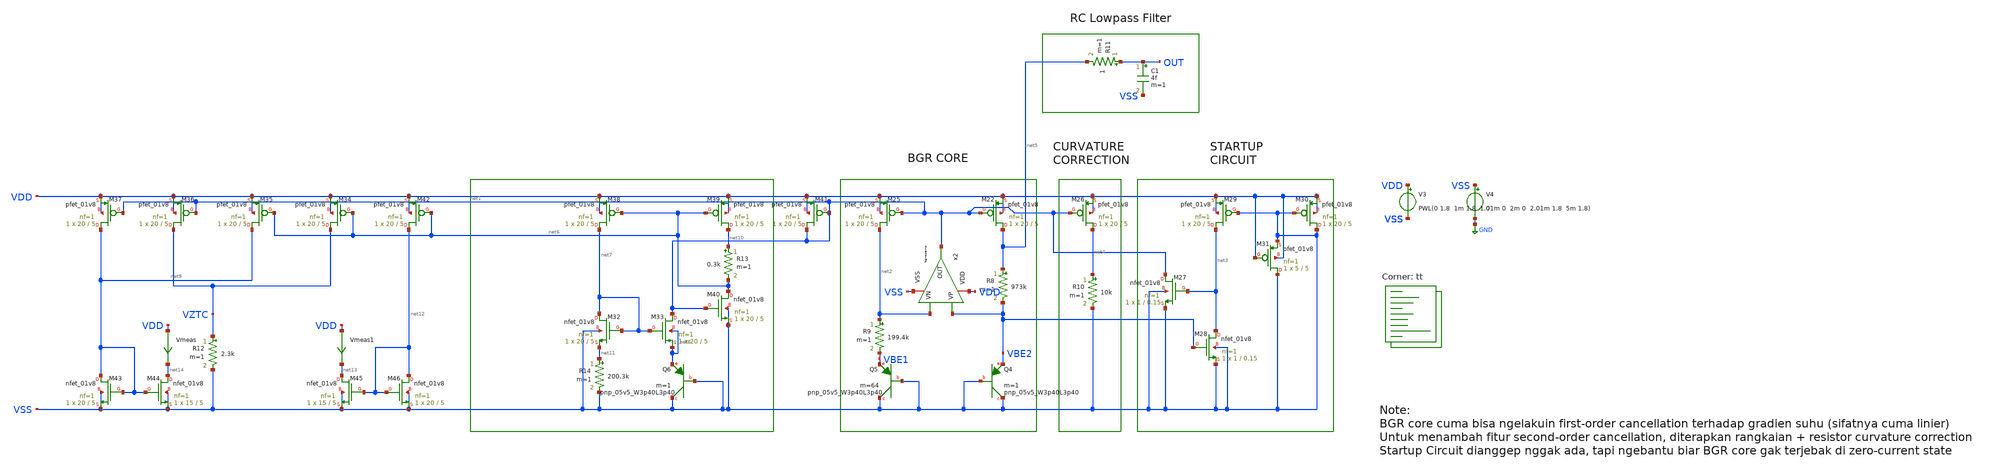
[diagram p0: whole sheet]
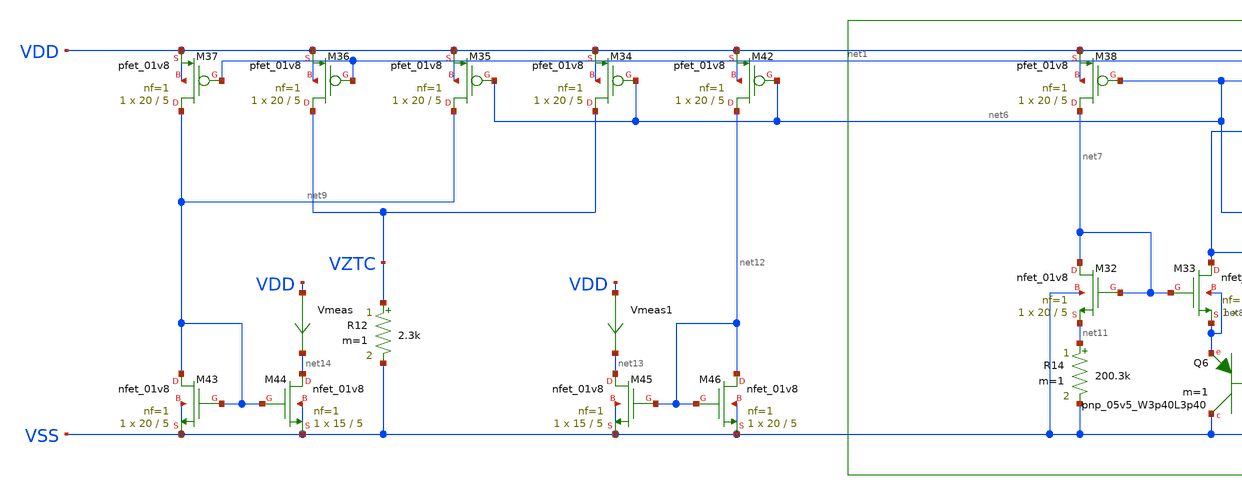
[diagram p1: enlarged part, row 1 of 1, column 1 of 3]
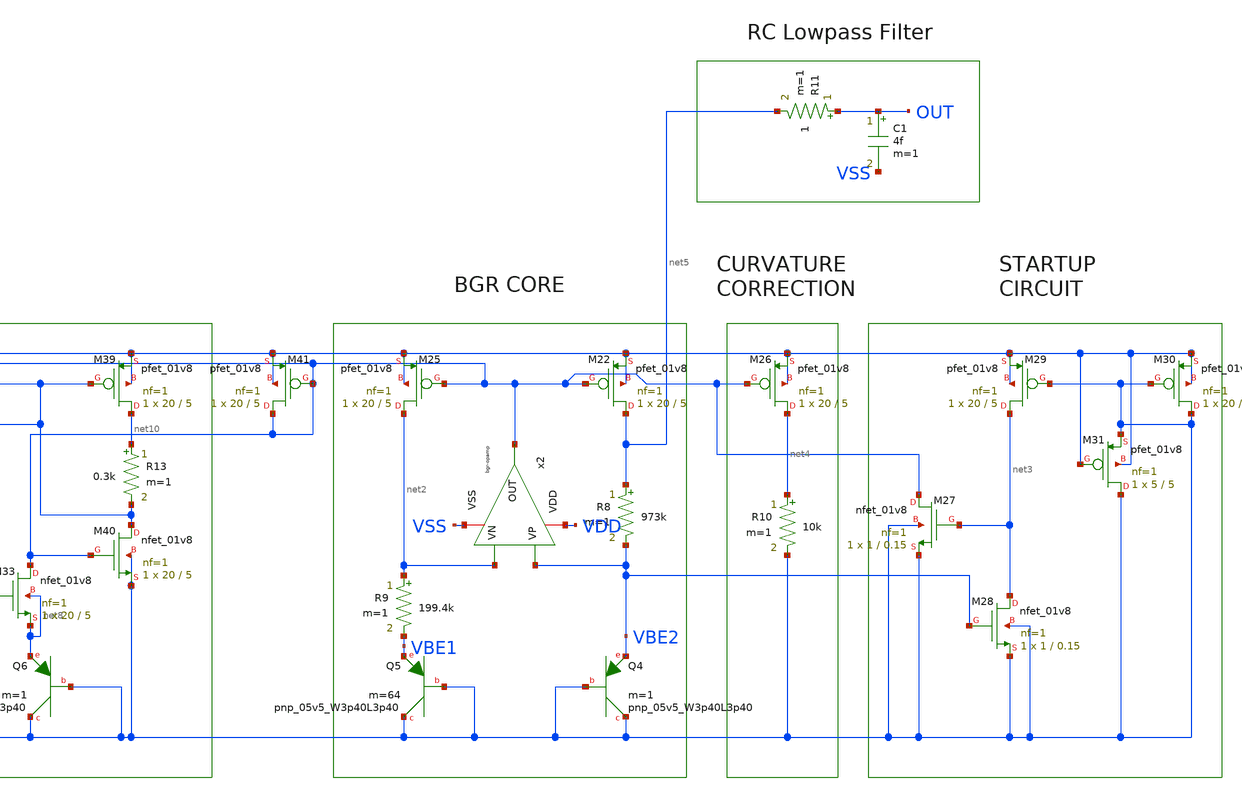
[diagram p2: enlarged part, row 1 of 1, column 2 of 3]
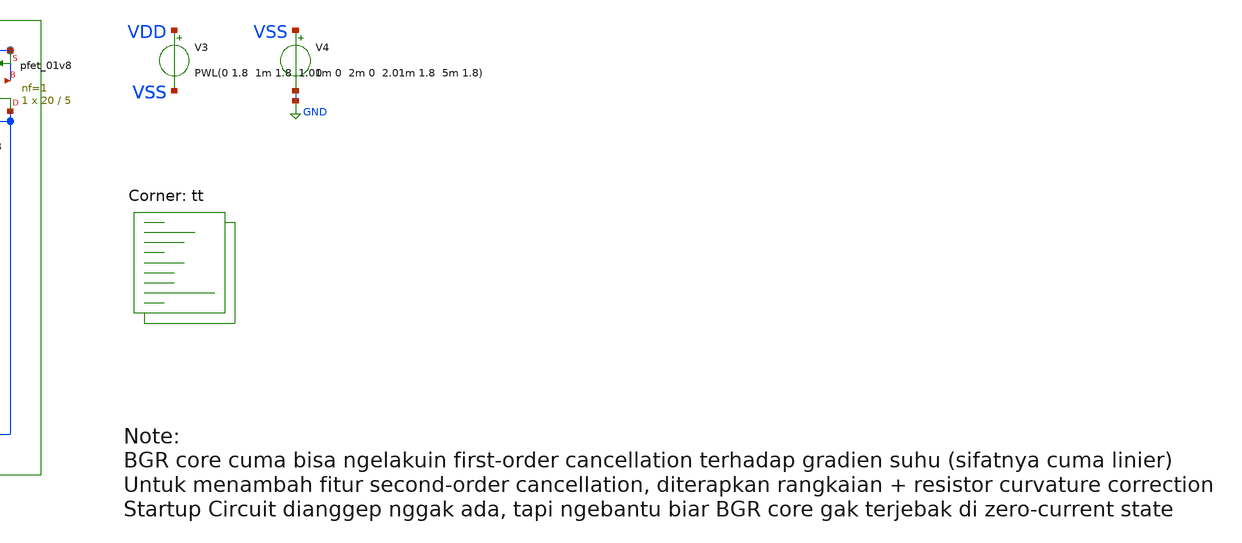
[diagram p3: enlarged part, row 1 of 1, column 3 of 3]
** sch_path: bandgap/bgr-final/tb_bgr-iref.sch
**.subckt tb_bgr-iref
V3 VDD VSS PWL(0 1.8 1m 1.8 1.01m 0 2m 0 2.01m 1.8 5m 1.8)
V4 VSS GND 0
x2 VDD net1 VBE2 net2 VSS bgr-opamp
XM22 net5 net1 VDD VDD sky130_fd_pr__pfet_01v8 L=5 W=20 nf=1 ad='int((nf+1)/2) * W/nf * 0.29' as='int((nf+2)/2) * W/nf * 0.29'
+ pd='2*int((nf+1)/2) * (W/nf + 0.29)' ps='2*int((nf+2)/2) * (W/nf + 0.29)' nrd='0.29 / W' nrs='0.29 / W'
+ sa=0 sb=0 sd=0 mult=1 m=1
XM25 net2 net1 VDD VDD sky130_fd_pr__pfet_01v8 L=5 W=20 nf=1 ad='int((nf+1)/2) * W/nf * 0.29' as='int((nf+2)/2) * W/nf * 0.29'
+ pd='2*int((nf+1)/2) * (W/nf + 0.29)' ps='2*int((nf+2)/2) * (W/nf + 0.29)' nrd='0.29 / W' nrs='0.29 / W'
+ sa=0 sb=0 sd=0 mult=1 m=1
R8 net5 VBE2 973k m=1
R9 net2 VBE1 199.4k m=1
XQ4 VSS VSS VBE2 sky130_fd_pr__pnp_05v5_W3p40L3p40 m=1
XQ5 VSS VSS VBE1 sky130_fd_pr__pnp_05v5_W3p40L3p40 m=64
XM26 net4 net1 VDD VDD sky130_fd_pr__pfet_01v8 L=5 W=20 nf=1 ad='int((nf+1)/2) * W/nf * 0.29' as='int((nf+2)/2) * W/nf * 0.29'
+ pd='2*int((nf+1)/2) * (W/nf + 0.29)' ps='2*int((nf+2)/2) * (W/nf + 0.29)' nrd='0.29 / W' nrs='0.29 / W'
+ sa=0 sb=0 sd=0 mult=1 m=1
R10 net4 VSS 10k m=1
XM27 net1 net3 VSS VSS sky130_fd_pr__nfet_01v8 L=0.15 W=1 nf=1 ad='int((nf+1)/2) * W/nf * 0.29' as='int((nf+2)/2) * W/nf * 0.29'
+ pd='2*int((nf+1)/2) * (W/nf + 0.29)' ps='2*int((nf+2)/2) * (W/nf + 0.29)' nrd='0.29 / W' nrs='0.29 / W'
+ sa=0 sb=0 sd=0 mult=1 m=1
XM28 net3 VBE2 VSS VSS sky130_fd_pr__nfet_01v8 L=0.15 W=1 nf=1 ad='int((nf+1)/2) * W/nf * 0.29' as='int((nf+2)/2) * W/nf * 0.29'
+ pd='2*int((nf+1)/2) * (W/nf + 0.29)' ps='2*int((nf+2)/2) * (W/nf + 0.29)' nrd='0.29 / W' nrs='0.29 / W'
+ sa=0 sb=0 sd=0 mult=1 m=1
XM29 net3 VSS VDD VDD sky130_fd_pr__pfet_01v8 L=5 W=20 nf=1 ad='int((nf+1)/2) * W/nf * 0.29' as='int((nf+2)/2) * W/nf * 0.29'
+ pd='2*int((nf+1)/2) * (W/nf + 0.29)' ps='2*int((nf+2)/2) * (W/nf + 0.29)' nrd='0.29 / W' nrs='0.29 / W'
+ sa=0 sb=0 sd=0 mult=1 m=1
XM30 VSS VSS VDD VDD sky130_fd_pr__pfet_01v8 L=5 W=20 nf=1 ad='int((nf+1)/2) * W/nf * 0.29' as='int((nf+2)/2) * W/nf * 0.29'
+ pd='2*int((nf+1)/2) * (W/nf + 0.29)' ps='2*int((nf+2)/2) * (W/nf + 0.29)' nrd='0.29 / W' nrs='0.29 / W'
+ sa=0 sb=0 sd=0 mult=1 m=1
XM31 VSS VDD VSS VDD sky130_fd_pr__pfet_01v8 L=5 W=5 nf=1 ad='int((nf+1)/2) * W/nf * 0.29' as='int((nf+2)/2) * W/nf * 0.29'
+ pd='2*int((nf+1)/2) * (W/nf + 0.29)' ps='2*int((nf+2)/2) * (W/nf + 0.29)' nrd='0.29 / W' nrs='0.29 / W'
+ sa=0 sb=0 sd=0 mult=1 m=1
C1 OUT VSS 4f m=1
R11 OUT net5 1 m=1
XM32 net7 net7 net11 VSS sky130_fd_pr__nfet_01v8 L=5 W=20 nf=1 ad='int((nf+1)/2) * W/nf * 0.29' as='int((nf+2)/2) * W/nf * 0.29'
+ pd='2*int((nf+1)/2) * (W/nf + 0.29)' ps='2*int((nf+2)/2) * (W/nf + 0.29)' nrd='0.29 / W' nrs='0.29 / W'
+ sa=0 sb=0 sd=0 mult=1 m=1
XM33 net1 net7 net8 net8 sky130_fd_pr__nfet_01v8 L=5 W=20 nf=1 ad='int((nf+1)/2) * W/nf * 0.29' as='int((nf+2)/2) * W/nf * 0.29'
+ pd='2*int((nf+1)/2) * (W/nf + 0.29)' ps='2*int((nf+2)/2) * (W/nf + 0.29)' nrd='0.29 / W' nrs='0.29 / W'
+ sa=0 sb=0 sd=0 mult=1 m=1
XQ6 VSS VSS net8 sky130_fd_pr__pnp_05v5_W3p40L3p40 m=1
XM34 VZTC net6 VDD VDD sky130_fd_pr__pfet_01v8 L=5 W=20 nf=1 ad='int((nf+1)/2) * W/nf * 0.29' as='int((nf+2)/2) * W/nf * 0.29'
+ pd='2*int((nf+1)/2) * (W/nf + 0.29)' ps='2*int((nf+2)/2) * (W/nf + 0.29)' nrd='0.29 / W' nrs='0.29 / W'
+ sa=0 sb=0 sd=0 mult=1 m=1
XM35 net9 net6 VDD VDD sky130_fd_pr__pfet_01v8 L=5 W=20 nf=1 ad='int((nf+1)/2) * W/nf * 0.29' as='int((nf+2)/2) * W/nf * 0.29'
+ pd='2*int((nf+1)/2) * (W/nf + 0.29)' ps='2*int((nf+2)/2) * (W/nf + 0.29)' nrd='0.29 / W' nrs='0.29 / W'
+ sa=0 sb=0 sd=0 mult=1 m=1
XM36 VZTC net1 VDD VDD sky130_fd_pr__pfet_01v8 L=5 W=20 nf=1 ad='int((nf+1)/2) * W/nf * 0.29' as='int((nf+2)/2) * W/nf * 0.29'
+ pd='2*int((nf+1)/2) * (W/nf + 0.29)' ps='2*int((nf+2)/2) * (W/nf + 0.29)' nrd='0.29 / W' nrs='0.29 / W'
+ sa=0 sb=0 sd=0 mult=1 m=1
XM37 net9 net1 VDD VDD sky130_fd_pr__pfet_01v8 L=5 W=20 nf=1 ad='int((nf+1)/2) * W/nf * 0.29' as='int((nf+2)/2) * W/nf * 0.29'
+ pd='2*int((nf+1)/2) * (W/nf + 0.29)' ps='2*int((nf+2)/2) * (W/nf + 0.29)' nrd='0.29 / W' nrs='0.29 / W'
+ sa=0 sb=0 sd=0 mult=1 m=1
R12 VZTC VSS 2.3k m=1
XM38 net7 net6 VDD VDD sky130_fd_pr__pfet_01v8 L=5 W=20 nf=1 ad='int((nf+1)/2) * W/nf * 0.29' as='int((nf+2)/2) * W/nf * 0.29'
+ pd='2*int((nf+1)/2) * (W/nf + 0.29)' ps='2*int((nf+2)/2) * (W/nf + 0.29)' nrd='0.29 / W' nrs='0.29 / W'
+ sa=0 sb=0 sd=0 mult=1 m=1
XM39 net10 net6 VDD VDD sky130_fd_pr__pfet_01v8 L=5 W=20 nf=1 ad='int((nf+1)/2) * W/nf * 0.29' as='int((nf+2)/2) * W/nf * 0.29'
+ pd='2*int((nf+1)/2) * (W/nf + 0.29)' ps='2*int((nf+2)/2) * (W/nf + 0.29)' nrd='0.29 / W' nrs='0.29 / W'
+ sa=0 sb=0 sd=0 mult=1 m=1
R13 net10 net6 0.3k m=1
XM40 net6 net1 VSS VSS sky130_fd_pr__nfet_01v8 L=5 W=20 nf=1 ad='int((nf+1)/2) * W/nf * 0.29' as='int((nf+2)/2) * W/nf * 0.29'
+ pd='2*int((nf+1)/2) * (W/nf + 0.29)' ps='2*int((nf+2)/2) * (W/nf + 0.29)' nrd='0.29 / W' nrs='0.29 / W'
+ sa=0 sb=0 sd=0 mult=1 m=1
XM41 net1 net1 VDD VDD sky130_fd_pr__pfet_01v8 L=5 W=20 nf=1 ad='int((nf+1)/2) * W/nf * 0.29' as='int((nf+2)/2) * W/nf * 0.29'
+ pd='2*int((nf+1)/2) * (W/nf + 0.29)' ps='2*int((nf+2)/2) * (W/nf + 0.29)' nrd='0.29 / W' nrs='0.29 / W'
+ sa=0 sb=0 sd=0 mult=1 m=1
R14 net11 VSS 200.3k m=1
XM42 net12 net6 VDD VDD sky130_fd_pr__pfet_01v8 L=5 W=20 nf=1 ad='int((nf+1)/2) * W/nf * 0.29' as='int((nf+2)/2) * W/nf * 0.29'
+ pd='2*int((nf+1)/2) * (W/nf + 0.29)' ps='2*int((nf+2)/2) * (W/nf + 0.29)' nrd='0.29 / W' nrs='0.29 / W'
+ sa=0 sb=0 sd=0 mult=1 m=1
XM43 net9 net9 VSS VSS sky130_fd_pr__nfet_01v8 L=5 W=20 nf=1 ad='int((nf+1)/2) * W/nf * 0.29' as='int((nf+2)/2) * W/nf * 0.29'
+ pd='2*int((nf+1)/2) * (W/nf + 0.29)' ps='2*int((nf+2)/2) * (W/nf + 0.29)' nrd='0.29 / W' nrs='0.29 / W'
+ sa=0 sb=0 sd=0 mult=1 m=1
XM44 net14 net9 VSS VSS sky130_fd_pr__nfet_01v8 L=5 W=15 nf=1 ad='int((nf+1)/2) * W/nf * 0.29' as='int((nf+2)/2) * W/nf * 0.29'
+ pd='2*int((nf+1)/2) * (W/nf + 0.29)' ps='2*int((nf+2)/2) * (W/nf + 0.29)' nrd='0.29 / W' nrs='0.29 / W'
+ sa=0 sb=0 sd=0 mult=1 m=1
XM45 net13 net12 VSS VSS sky130_fd_pr__nfet_01v8 L=5 W=15 nf=1 ad='int((nf+1)/2) * W/nf * 0.29' as='int((nf+2)/2) * W/nf * 0.29'
+ pd='2*int((nf+1)/2) * (W/nf + 0.29)' ps='2*int((nf+2)/2) * (W/nf + 0.29)' nrd='0.29 / W' nrs='0.29 / W'
+ sa=0 sb=0 sd=0 mult=1 m=1
XM46 net12 net12 VSS VSS sky130_fd_pr__nfet_01v8 L=5 W=20 nf=1 ad='int((nf+1)/2) * W/nf * 0.29' as='int((nf+2)/2) * W/nf * 0.29'
+ pd='2*int((nf+1)/2) * (W/nf + 0.29)' ps='2*int((nf+2)/2) * (W/nf + 0.29)' nrd='0.29 / W' nrs='0.29 / W'
+ sa=0 sb=0 sd=0 mult=1 m=1
Vmeas VDD net14 0
.save i(vmeas)
Vmeas1 VDD net13 0
.save i(vmeas1)
**** begin user architecture code
.lib $::SKYWATER_MODELS/sky130.lib.spice tt



.control
  set noaskquit
  set numdgt=10
  save all

  * =========================
  * TRANSIENT: Iref health test
  * =========================

  * ---- 0) Pastikan starting condition keras (biar kelihatan startup beneran)
  * uic = skip operating point, start from ICs (lebih brutal)
  * Kalau terlalu brutal dan gagal konvergen, ganti uic -> tanpa uic
  * (Optional) kamu juga bisa set .ic node tertentu di netlist

  * ---- 1) Run transient startup
  tran 1u 5m uic

  * ---- 2) Definisi arus Iref (ubah sesuai arah yg lu mau)
  * Biasanya: Iref = -i(Vmeas) supaya keluar node jadi positif
  let Iref  = i(vmeas)
  let Iref1 = i(vmeas1)

  * ---- 3) Ukur Iref steady-state (ambil nilai mendekati akhir simulasi)
  meas tran Iref_ss  avg Iref  from=4m to=5m
  meas tran Iref1_ss avg Iref1 from=4m to=5m

  * ---- 4) Waktu settle ke 1% (health metric)
  * Def: waktu pertama kali Iref masuk band +/-1% dari steady dan stay (approx)
  let Iref_hi = 1.01*Iref_ss
  let Iref_lo = 0.99*Iref_ss

  meas tran t_settle_hi when Iref = Iref_hi rise=1
  meas tran t_settle_lo when Iref = Iref_lo rise=1

  * ---- 5) Overshoot/undershoot
  meas tran Iref_max max Iref from=0 to=5m
  meas tran Iref_min min Iref from=0 to=5m

  * ---- 6) “Wrong state” detector: apakah sempat nyangkut di ~0?
  * (threshold bisa kamu ubah)
  meas tran t_first_1u when Iref = 1u rise=1

  echo ==== Iref transient health (startup) ====
  print Iref_ss Iref_max Iref_min t_first_1u t_settle_lo t_settle_hi
  print Iref1_ss

  plot Iref
  plot Iref1
  plot v(out)

.endc


**** end user architecture code
**.ends

* expanding   symbol:  afe-icdec-teknofest-2026/bandgap/bgr-opamp/bgr-opamp.sym # of pins=5
** sym_path: bandgap/bgr-opamp/bgr-opamp.sym
** sch_path: bandgap/bgr-opamp/bgr-opamp.sch
.subckt bgr-opamp VDD OUT VP VN VSS
*.iopin VSS
*.iopin VDD
*.ipin VP
*.ipin VN
*.opin OUT
XM1 net1 VP net3 VSS sky130_fd_pr__nfet_01v8 L=0.3 W=2.5 nf=2 ad='int((nf+1)/2) * W/nf * 0.29' as='int((nf+2)/2) * W/nf * 0.29'
+ pd='2*int((nf+1)/2) * (W/nf + 0.29)' ps='2*int((nf+2)/2) * (W/nf + 0.29)' nrd='0.29 / W' nrs='0.29 / W'
+ sa=0 sb=0 sd=0 mult=1 m=1
XM2 net2 VN net3 VSS sky130_fd_pr__nfet_01v8 L=0.3 W=2.5 nf=2 ad='int((nf+1)/2) * W/nf * 0.29' as='int((nf+2)/2) * W/nf * 0.29'
+ pd='2*int((nf+1)/2) * (W/nf + 0.29)' ps='2*int((nf+2)/2) * (W/nf + 0.29)' nrd='0.29 / W' nrs='0.29 / W'
+ sa=0 sb=0 sd=0 mult=1 m=1
XM4 net2 net1 VDD VDD sky130_fd_pr__pfet_01v8 L=1.25 W=10.8 nf=4 ad='int((nf+1)/2) * W/nf * 0.29' as='int((nf+2)/2) * W/nf * 0.29'
+ pd='2*int((nf+1)/2) * (W/nf + 0.29)' ps='2*int((nf+2)/2) * (W/nf + 0.29)' nrd='0.29 / W' nrs='0.29 / W'
+ sa=0 sb=0 sd=0 mult=1 m=1
XM3 net1 net1 VDD VDD sky130_fd_pr__pfet_01v8 L=1.25 W=10.8 nf=4 ad='int((nf+1)/2) * W/nf * 0.29' as='int((nf+2)/2) * W/nf * 0.29'
+ pd='2*int((nf+1)/2) * (W/nf + 0.29)' ps='2*int((nf+2)/2) * (W/nf + 0.29)' nrd='0.29 / W' nrs='0.29 / W'
+ sa=0 sb=0 sd=0 mult=1 m=1
XM5 net3 net4 VSS VSS sky130_fd_pr__nfet_01v8 L=1.25 W=3.4 nf=1 ad='int((nf+1)/2) * W/nf * 0.29' as='int((nf+2)/2) * W/nf * 0.29'
+ pd='2*int((nf+1)/2) * (W/nf + 0.29)' ps='2*int((nf+2)/2) * (W/nf + 0.29)' nrd='0.29 / W' nrs='0.29 / W'
+ sa=0 sb=0 sd=0 mult=1 m=1
XM9 net4 net5 net10 VSS sky130_fd_pr__nfet_01v8 L=1.25 W=3.4 nf=1 ad='int((nf+1)/2) * W/nf * 0.29' as='int((nf+2)/2) * W/nf * 0.29'
+ pd='2*int((nf+1)/2) * (W/nf + 0.29)' ps='2*int((nf+2)/2) * (W/nf + 0.29)' nrd='0.29 / W' nrs='0.29 / W'
+ sa=0 sb=0 sd=0 mult=1 m=1
XM8 net4 net4 VDD VDD sky130_fd_pr__pfet_01v8 L=1.25 W=10.8 nf=4 ad='int((nf+1)/2) * W/nf * 0.29' as='int((nf+2)/2) * W/nf * 0.29'
+ pd='2*int((nf+1)/2) * (W/nf + 0.29)' ps='2*int((nf+2)/2) * (W/nf + 0.29)' nrd='0.29 / W' nrs='0.29 / W'
+ sa=0 sb=0 sd=0 mult=1 m=1
XM11 net5 net4 VDD VDD sky130_fd_pr__pfet_01v8 L=1.25 W=10.8 nf=4 ad='int((nf+1)/2) * W/nf * 0.29' as='int((nf+2)/2) * W/nf * 0.29'
+ pd='2*int((nf+1)/2) * (W/nf + 0.29)' ps='2*int((nf+2)/2) * (W/nf + 0.29)' nrd='0.29 / W' nrs='0.29 / W'
+ sa=0 sb=0 sd=0 mult=1 m=1
XM10 net5 net5 VSS VSS sky130_fd_pr__nfet_01v8 L=1.25 W=3.4 nf=1 ad='int((nf+1)/2) * W/nf * 0.29' as='int((nf+2)/2) * W/nf * 0.29'
+ pd='2*int((nf+1)/2) * (W/nf + 0.29)' ps='2*int((nf+2)/2) * (W/nf + 0.29)' nrd='0.29 / W' nrs='0.29 / W'
+ sa=0 sb=0 sd=0 mult=1 m=1
XM6 OUT net2 VDD VDD sky130_fd_pr__pfet_01v8 L=1.25 W=110 nf=32 ad='int((nf+1)/2) * W/nf * 0.29' as='int((nf+2)/2) * W/nf * 0.29'
+ pd='2*int((nf+1)/2) * (W/nf + 0.29)' ps='2*int((nf+2)/2) * (W/nf + 0.29)' nrd='0.29 / W' nrs='0.29 / W'
+ sa=0 sb=0 sd=0 mult=1 m=1
XM7 OUT net4 VSS VSS sky130_fd_pr__nfet_01v8 L=1.25 W=12 nf=4 ad='int((nf+1)/2) * W/nf * 0.29' as='int((nf+2)/2) * W/nf * 0.29'
+ pd='2*int((nf+1)/2) * (W/nf + 0.29)' ps='2*int((nf+2)/2) * (W/nf + 0.29)' nrd='0.29 / W' nrs='0.29 / W'
+ sa=0 sb=0 sd=0 mult=1 m=1
XC2 OUT net2 sky130_fd_pr__cap_mim_m3_1 W=15 L=15 MF=4 m=4
XM12 net4 net4 net5 VSS sky130_fd_pr__nfet_01v8 L=0.15 W=0.85 nf=1 ad='int((nf+1)/2) * W/nf * 0.29' as='int((nf+2)/2) * W/nf * 0.29'
+ pd='2*int((nf+1)/2) * (W/nf + 0.29)' ps='2*int((nf+2)/2) * (W/nf + 0.29)' nrd='0.29 / W' nrs='0.29 / W'
+ sa=0 sb=0 sd=0 mult=1 m=1
XR2 net6 net10 VSS sky130_fd_pr__res_high_po_1p41 L=3.235 mult=1 m=1
XR3 net8 net6 VSS sky130_fd_pr__res_high_po_1p41 L=3.235 mult=1 m=1
XR4 net7 net8 VSS sky130_fd_pr__res_high_po_1p41 L=3.235 mult=1 m=1
XR5 net9 net7 VSS sky130_fd_pr__res_high_po_1p41 L=3.235 mult=1 m=1
XR6 VSS net9 VSS sky130_fd_pr__res_high_po_1p41 L=3.235 mult=1 m=1
.ends

.GLOBAL GND
.end
